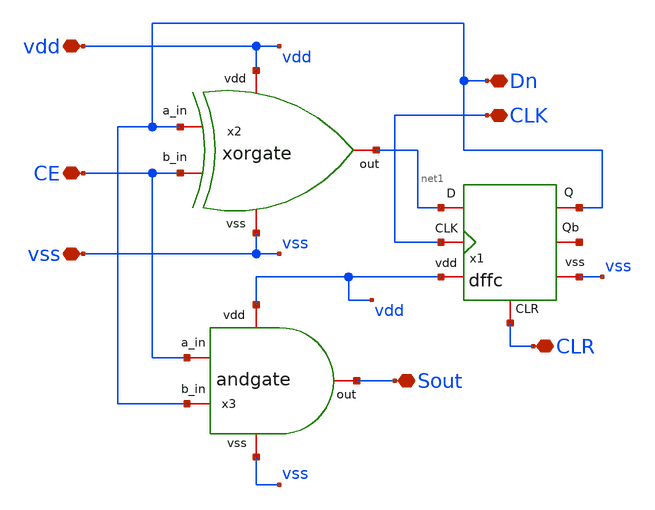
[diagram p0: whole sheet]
** sch_path: design/blocks/count1bit/schematic/count1bit.sch
**.subckt count1bit Dn CLK CLR Sout vss CE vdd
*.iopin Dn
*.iopin CLK
*.iopin CLR
*.iopin Sout
*.iopin vss
*.iopin CE
*.iopin vdd
x1 net1 Dn CLR net2 vdd CLK vss dffc
x2 vdd net1 vss Dn CE xorgate
x3 vdd CE Sout Dn vss andgate
**.ends
.end
